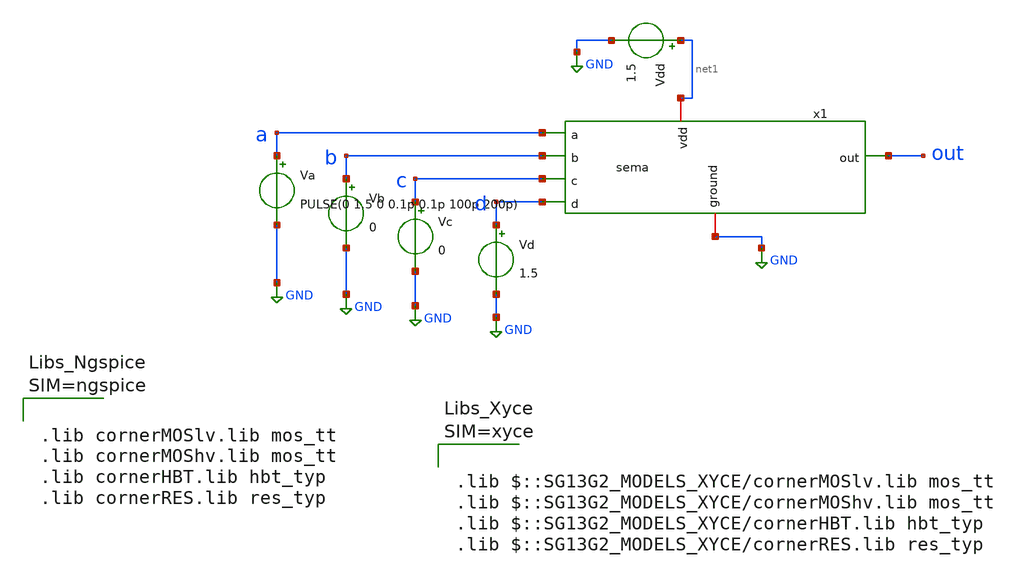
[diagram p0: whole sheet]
** sch_path: projekat/slucaj_1_8/tb_tran.sch
**.subckt tb_tran
Va a GND PULSE(0 1.5 0 0.1p 0.1p 100p 200p)
Vb b GND 0
Vc c GND 0
Vd d GND 1.5
Vdd net1 GND 1.5
x1 net1 out d a c b GND sema
**** begin user architecture code



.lib cornerMOSlv.lib mos_tt
.lib cornerMOShv.lib mos_tt
.lib cornerHBT.lib hbt_typ
.lib cornerRES.lib res_typ









.tran 0.1p 500p

.control
  save all
  run

  meas tran tr_out TRIG v(out) VAL=0.15 RISE=2 TARG v(out) VAL=1.35 RISE=2
  meas tran tf_out TRIG v(out) VAL=1.35 FALL=2 TARG v(out) VAL=0.15 FALL=2

  plot v(a)+6 v(b)+4.5 v(c)+3 v(d)+1.5 v(out)
  print tr_out tf_out
  wrdata najgori_odziv_1_8.txt v(a) v(out)
.endc

**** end user architecture code
**.ends

* expanding   symbol:  /home/Nikola.Jankovic/projekat/slucaj_1_8/sema.sym # of pins=7
** sym_path: projekat/slucaj_1_8/sema.sym
** sch_path: projekat/slucaj_1_8/sema.sch
.subckt sema vdd out d a c b ground
*.ipin a
*.ipin b
*.ipin c
*.ipin d
*.iopin vdd
*.iopin ground
*.opin out
XM1 net1 a ground ground sg13_lv_nmos w=0.3u l=0.13u ng=1 m=1 mm_ok=1
XM2 net1 b ground ground sg13_lv_nmos w=0.3u l=0.13u ng=1 m=1 mm_ok=1
XM3 net1 c ground ground sg13_lv_nmos w=0.3u l=0.13u ng=1 m=1 mm_ok=1
XM4 out d net1 ground sg13_lv_nmos w=0.3u l=0.13u ng=1 m=1 mm_ok=1
XM5 net2 a vdd vdd sg13_lv_pmos w=0.81u l=0.13u ng=1 m=1 mm_ok=1
XM6 net3 b net2 vdd sg13_lv_pmos w=0.81u l=0.13u ng=1 m=1 mm_ok=1
XM7 out c net3 vdd sg13_lv_pmos w=0.81u l=0.13u ng=1 m=1 mm_ok=1
XM8 out d vdd vdd sg13_lv_pmos w=0.27u l=0.13u ng=1 m=1 mm_ok=1
.ends

.GLOBAL GND
.end
